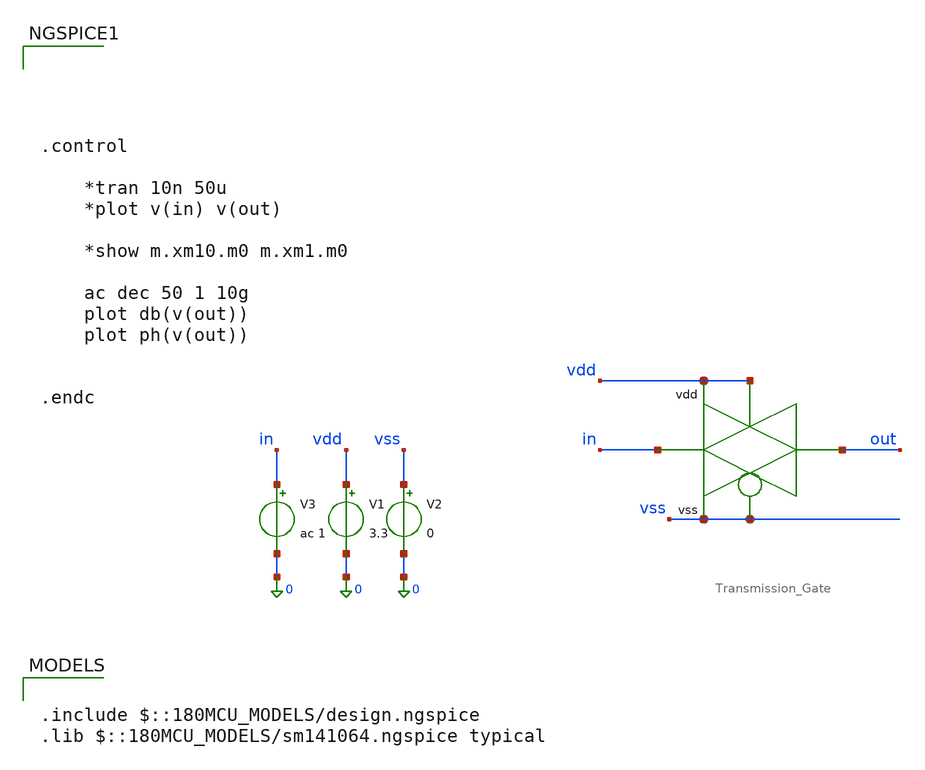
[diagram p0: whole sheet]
** sch_path: simulation/testbench_analog/TG/TG_freq-response.sch
**.subckt TG_freq-response
x1 in vss vdd vdd vss out Transmission_Gate
V1 vdd 0 3.3
V2 vss 0 0
V3 in 0 ac 1
**** begin user architecture code

.include $::180MCU_MODELS/design.ngspice
.lib $::180MCU_MODELS/sm141064.ngspice typical






.control

	*tran 10n 50u
	*plot v(in) v(out)

	*show m.xm10.m0 m.xm1.m0

	ac dec 50 1 10g
	plot db(v(out))
	plot ph(v(out))


.endc


**** end user architecture code
**.ends

* expanding   symbol:  Transmission_Gate.sym # of pins=6
** sym_path: design/analog/transmission_gate/Transmission_Gate.sym
** sch_path: design/analog/transmission_gate/Transmission_Gate.sch
.subckt Transmission_Gate A en_b en vdd vss B
*.ipin en_b
*.iopin A
*.iopin B
*.ipin en
*.iopin vdd
*.iopin vss
XM1 B en_b A vdd pfet_03v3 L=0.28u W=20u nf=10 ad='int((nf+1)/2) * W/nf * 0.18u' as='int((nf+2)/2) * W/nf * 0.18u'
+ pd='2*int((nf+1)/2) * (W/nf + 0.18u)' ps='2*int((nf+2)/2) * (W/nf + 0.18u)' nrd='0.18u / W' nrs='0.18u / W'
+ sa=0 sb=0 sd=0 m=8
XM2 A en B vss nfet_03v3 L=0.28u W=10u nf=5 ad='int((nf+1)/2) * W/nf * 0.18u' as='int((nf+2)/2) * W/nf * 0.18u'
+ pd='2*int((nf+1)/2) * (W/nf + 0.18u)' ps='2*int((nf+2)/2) * (W/nf + 0.18u)' nrd='0.18u / W' nrs='0.18u / W'
+ sa=0 sb=0 sd=0 m=8
.ends

.end
